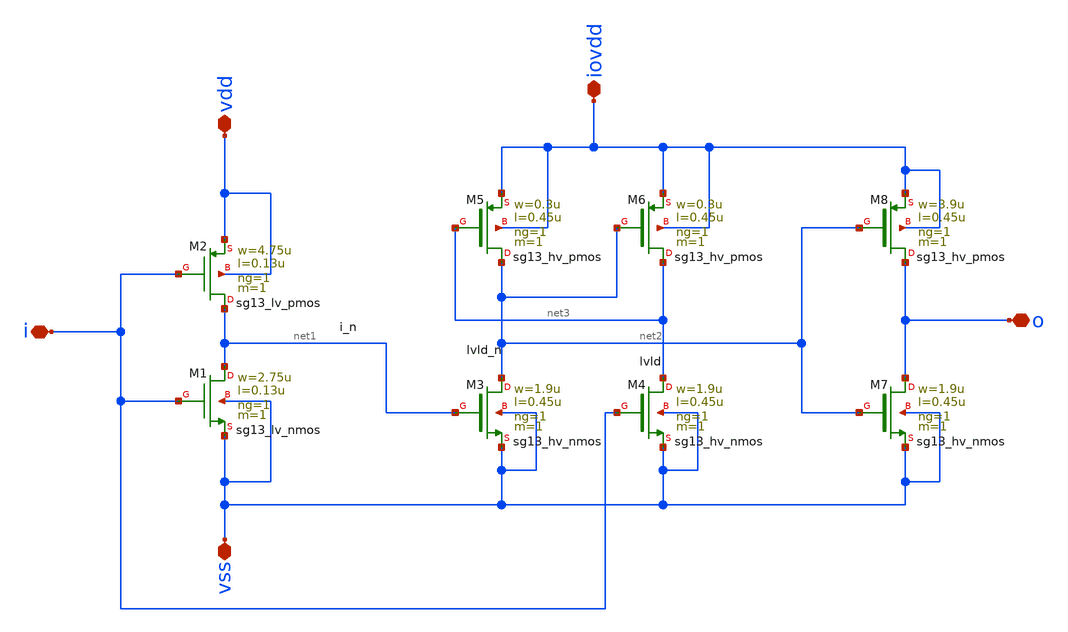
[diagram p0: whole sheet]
** sch_path: ihp-sg13g2/libs.ref/sg13g2_io/xschem/sg13g2_LevelUpInv.sch
**.subckt sg13g2_LevelUpInv i vss vdd iovdd o
*.iopin i
*.iopin vss
*.iopin vdd
*.iopin iovdd
*.iopin o
XM1 net1 i vss vss sg13_lv_nmos w=2.75u l=0.13u ng=1 m=1
XM2 net1 i vdd vdd sg13_lv_pmos w=4.75u l=0.13u ng=1 m=1
XM3 net2 net1 vss vss sg13_hv_nmos w=1.9u l=0.45u ng=1 m=1
XM4 net3 i vss vss sg13_hv_nmos w=1.9u l=0.45u ng=1 m=1
XM5 net2 net3 iovdd iovdd sg13_hv_pmos w=0.3u l=0.45u ng=1 m=1
XM6 net3 net2 iovdd iovdd sg13_hv_pmos w=0.3u l=0.45u ng=1 m=1
XM7 o net2 vss vss sg13_hv_nmos w=1.9u l=0.45u ng=1 m=1
XM8 o net2 iovdd iovdd sg13_hv_pmos w=3.9u l=0.45u ng=1 m=1
**.ends
.end
